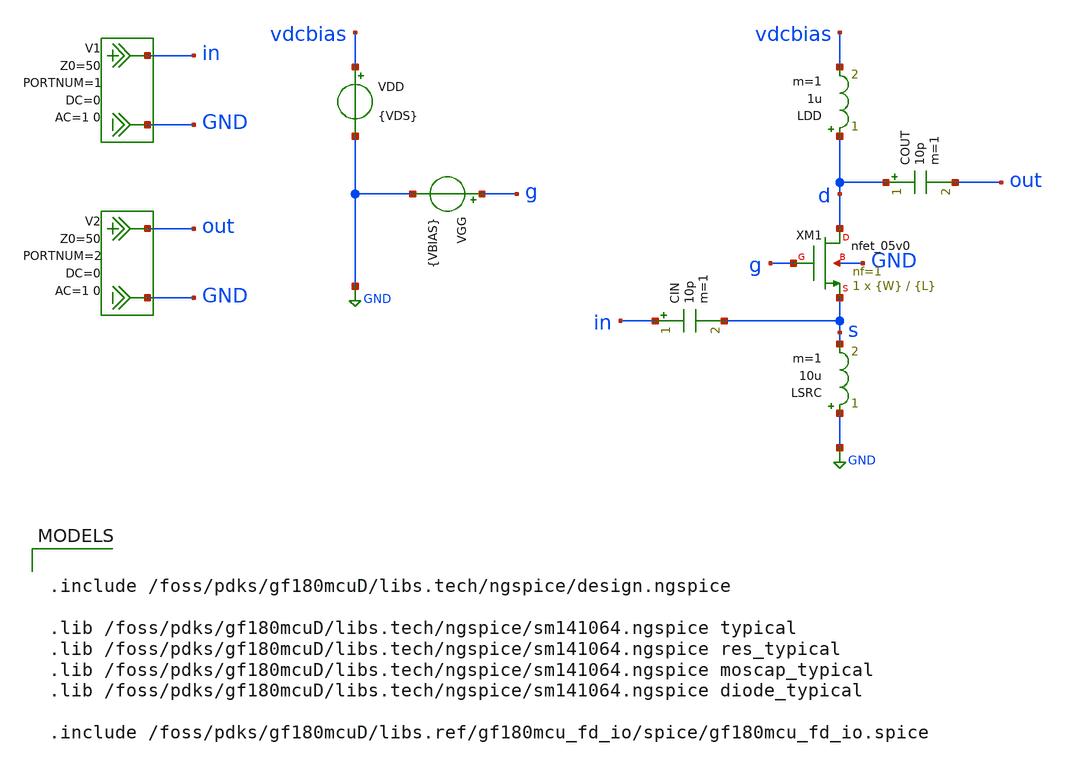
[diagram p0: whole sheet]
** sch_path: NFmin_Simulation/simulations/05v0/nfmin_jd_nmos_cg_05.sch
**.subckt nfmin_jd_nmos_cg_05
VGG g GND {VBIAS}
VDD vdcbias GND {VDS}
LDD d vdcbias 1u m=1
COUT d out 10p m=1
CIN in s 10p m=1
V1 in GND DC 0 AC 1 0 portnum 1 z0 50
V2 out GND DC 0 AC 1 0 portnum 2 z0 50
LSRC GND s 10u m=1
XM1 d g s GND nfet_05v0 L={L} W={W} nf=1 ad='int((nf+1)/2) * W/nf * 0.18u' as='int((nf+2)/2) * W/nf * 0.18u'
+ pd='2*int((nf+1)/2) * (W/nf + 0.18u)' ps='2*int((nf+2)/2) * (W/nf + 0.18u)' nrd='0.18u / W' nrs='0.18u / W'
+ sa=0 sb=0 sd=0 m=1
**** begin user architecture code

.include /foss/pdks/gf180mcuD/libs.tech/ngspice/design.ngspice

.lib /foss/pdks/gf180mcuD/libs.tech/ngspice/sm141064.ngspice typical
.lib /foss/pdks/gf180mcuD/libs.tech/ngspice/sm141064.ngspice res_typical
.lib /foss/pdks/gf180mcuD/libs.tech/ngspice/sm141064.ngspice moscap_typical
.lib /foss/pdks/gf180mcuD/libs.tech/ngspice/sm141064.ngspice diode_typical

.include /foss/pdks/gf180mcuD/libs.ref/gf180mcu_fd_io/spice/gf180mcu_fd_io.spice




.option savecurrents

.param fnoicor=0
.param sw_stat_mismatch=0

.param VBIAS=0.9
.param VDS=5.0

.param W=0.30e-6
.param L=0.70e-6

.control
  set noaskquit

  echo VDS_set_V W_m L_m VBIAS_set_V VGS_actual_V VDS_actual_V VBS_actual_V ID_A JD_mA_per_um Pdc_mW
+ gm_S gds_S gm_ID_1_per_V ro_Ohm gmro Rin_CG_est_Ohm NFmin_dB NF_dB Rn_Ohm SOpt_real SOpt_imag SOpt_mag >
+ nmos05_cg_full_nom5v.txt

  foreach vdsval 5.0

    foreach wval 0.30e-6 1e-6 5e-6 10e-6 20e-6 50e-6

      foreach lval 0.60e-6 0.70e-6 1.00e-6

        setplot const
        let k = 0

        while k <= 400

          setplot const
          let vbias = 0.50 + 0.005*k

          alterparam VDS = $vdsval
          alterparam W = $wval
          alterparam L = $lval
          alterparam VBIAS = $&vbias
          reset

          op

          let idn_tmp = abs(i(vdd))
          let jd_tmp = 1e-3*idn_tmp/$wval
          let pdc_tmp = 1e3*idn_tmp*$vdsval

          let vgs_tmp = v(g)-v(s)
          let vds_tmp = v(d)-v(s)
          let vbs_tmp = -v(s)

          let gm_tmp = @m.xm1.m0[gm]
          let gds_tmp = @m.xm1.m0[gds]

          let gm_id_tmp = gm_tmp/idn_tmp
          let ro_tmp = 1/gds_tmp
          let gmro_tmp = gm_tmp/gds_tmp
          let rin_cg_tmp = 1/gm_tmp

          set idn_op = $&idn_tmp
          set jd_op = $&jd_tmp
          set pdc_op = $&pdc_tmp
          set vgs_op = $&vgs_tmp
          set vds_op = $&vds_tmp
          set vbs_op = $&vbs_tmp
          set gm_op = $&gm_tmp
          set gds_op = $&gds_tmp
          set gm_id_op = $&gm_id_tmp
          set ro_op = $&ro_tmp
          set gmro_op = $&gmro_tmp
          set rin_cg_op = $&rin_cg_tmp

          destroy $curplot

          sp lin 1 2.4e9 2.4e9 1

          let nfmin_val = real(NFmin)
          let nf_val = real(NF)
          let rn_val = real(Rn)
          let sopt_re = real(SOpt)
          let sopt_im = imag(SOpt)
          let sopt_mag = sqrt(sopt_re*sopt_re + sopt_im*sopt_im)

          echo $vdsval $wval $lval $&vbias $vgs_op $vds_op $vbs_op $idn_op $jd_op $pdc_op $gm_op
+ $gds_op $gm_id_op $ro_op $gmro_op $rin_cg_op $&nfmin_val $&nf_val $&rn_val $&sopt_re $&sopt_im $&sopt_mag
+ >> nmos05_cg_full_nom5v.txt

          destroy $curplot

          setplot const
          let k = k + 1

        end

      end

    end

  end

.endc


**** end user architecture code
**.ends
.GLOBAL GND
.end
